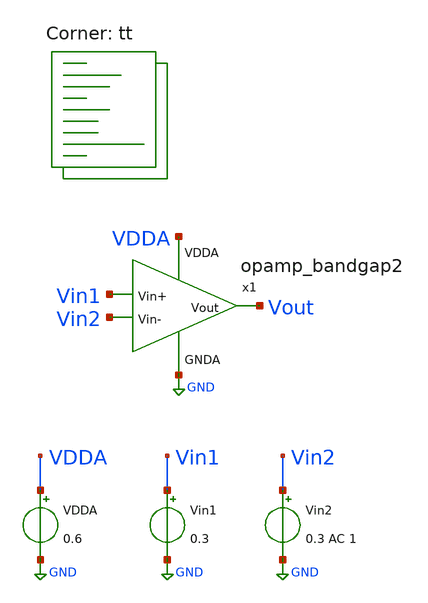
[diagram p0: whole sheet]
** sch_path: projects/pll/bandgapref/xschem_ngspice/tb_opamp_bandgap.sch
**.subckt tb_opamp_bandgap
VDDA VDDA GND 0.6
Vin1 Vin1 GND 0.3
Vin2 Vin2 GND 0.3 AC 1
x1 VDDA Vout Vin2 Vin1 GND opamp_bandgap2
**** begin user architecture code



.option wnflag=1

* .param VDDGAUSS = agauss(1.8, 0.05, 1)
* .param VDD = VDDGAUSS
* .param VDD = 1.8

* .param TEMPGAUSS = agauss(40, 30, 1)
* .param temp = TEMPGAUSS
.option temp = 26

.control

  save all
   *tran 1u 20m
   ac dec 20 1 1T

  write tb_opamp_bandgap.raw
  set appendwrite

.endc



.lib $::SKYWATER_MODELS/sky130.lib.spice tt
**** end user architecture code
**.ends

* expanding   symbol:
*+  /foss/designs/my_design/projects/pll/bandgapref/xschem_ngspice/opamp_bandgap2.sym # of pins=5
** sym_path: projects/bandgapref/xschem_ngspice/old_files/opamp_bandgap2.sym
** sch_path: projects/bandgapref/xschem_ngspice/old_files/opamp_bandgap2.sch
.subckt opamp_bandgap2 VDDA Vout Vin- Vin+ GNDA
*.ipin Vin+
*.opin Vout
*.ipin Vin-
*.ipin GNDA
*.ipin VDDA
XM2 net2 Vin- net1 GNDA sky130_fd_pr__nfet_01v8 L=0.6 W=2 nf=2 ad='int((nf+1)/2) * W/nf * 0.29' as='int((nf+2)/2) * W/nf * 0.29'
+ pd='2*int((nf+1)/2) * (W/nf + 0.29)' ps='2*int((nf+2)/2) * (W/nf + 0.29)' nrd='0.29 / W' nrs='0.29 / W'
+ sa=0 sb=0 sd=0 mult=1 m=1
XM3 Vout Vin+ net1 GNDA sky130_fd_pr__nfet_01v8 L=0.6 W=2 nf=2 ad='int((nf+1)/2) * W/nf * 0.29' as='int((nf+2)/2) * W/nf * 0.29'
+ pd='2*int((nf+1)/2) * (W/nf + 0.29)' ps='2*int((nf+2)/2) * (W/nf + 0.29)' nrd='0.29 / W' nrs='0.29 / W'
+ sa=0 sb=0 sd=0 mult=1 m=1
XM1 net1 net1 GNDA GNDA sky130_fd_pr__nfet_01v8 L=0.6 W=4 nf=1 ad='int((nf+1)/2) * W/nf * 0.29' as='int((nf+2)/2) * W/nf * 0.29'
+ pd='2*int((nf+1)/2) * (W/nf + 0.29)' ps='2*int((nf+2)/2) * (W/nf + 0.29)' nrd='0.29 / W' nrs='0.29 / W'
+ sa=0 sb=0 sd=0 mult=1 m=1
XM4 Vout net2 VDDA VDDA sky130_fd_pr__pfet_01v8 L=0.6 W=4 nf=4 ad='int((nf+1)/2) * W/nf * 0.29' as='int((nf+2)/2) * W/nf * 0.29'
+ pd='2*int((nf+1)/2) * (W/nf + 0.29)' ps='2*int((nf+2)/2) * (W/nf + 0.29)' nrd='0.29 / W' nrs='0.29 / W'
+ sa=0 sb=0 sd=0 mult=1 m=1
XM5 net2 net2 VDDA VDDA sky130_fd_pr__pfet_01v8 L=0.6 W=4 nf=4 ad='int((nf+1)/2) * W/nf * 0.29' as='int((nf+2)/2) * W/nf * 0.29'
+ pd='2*int((nf+1)/2) * (W/nf + 0.29)' ps='2*int((nf+2)/2) * (W/nf + 0.29)' nrd='0.29 / W' nrs='0.29 / W'
+ sa=0 sb=0 sd=0 mult=1 m=1
.ends

.GLOBAL GND
.end
